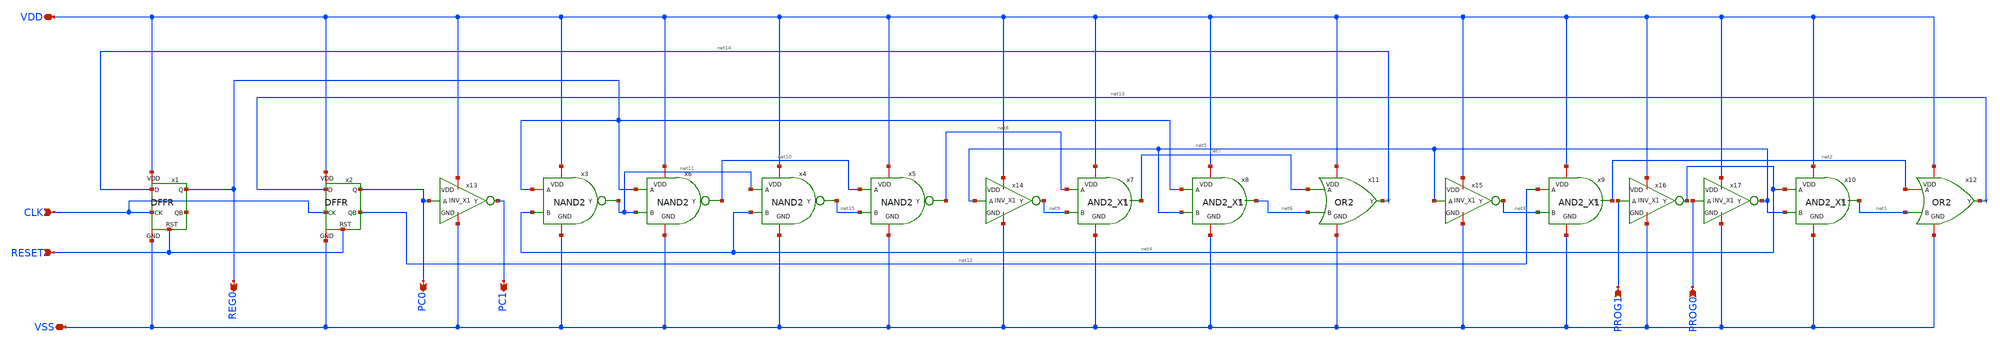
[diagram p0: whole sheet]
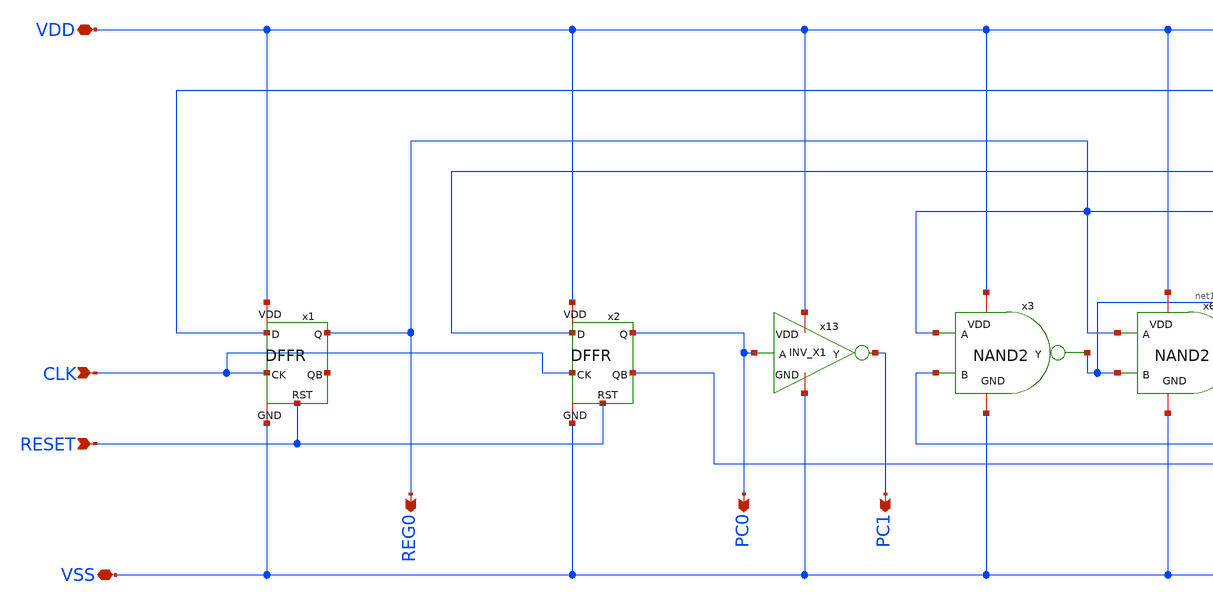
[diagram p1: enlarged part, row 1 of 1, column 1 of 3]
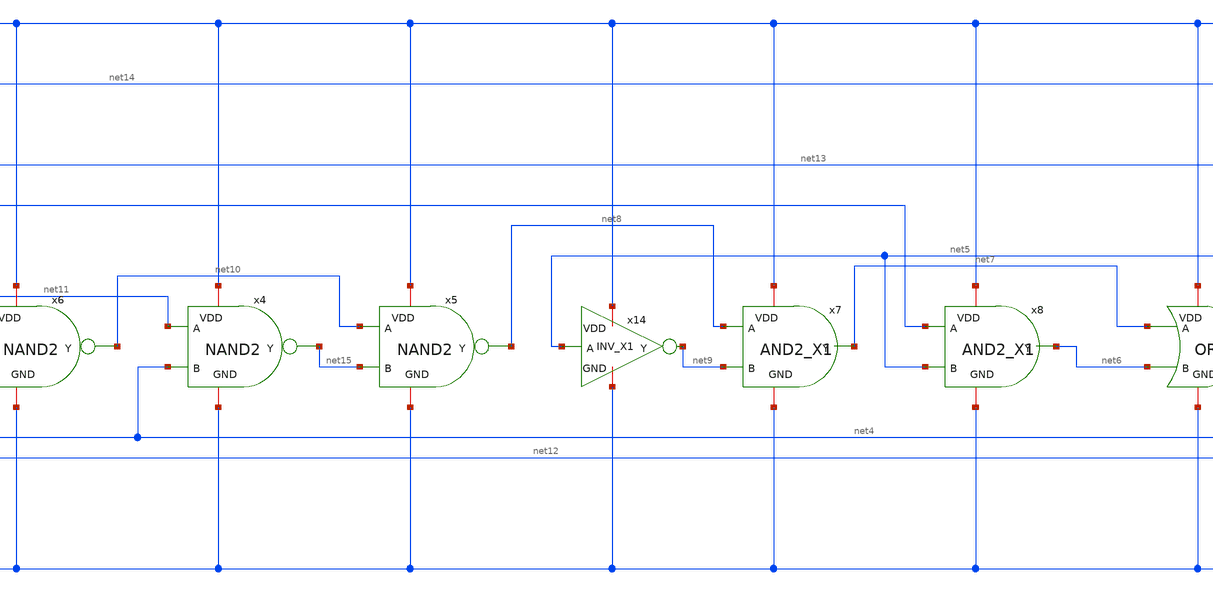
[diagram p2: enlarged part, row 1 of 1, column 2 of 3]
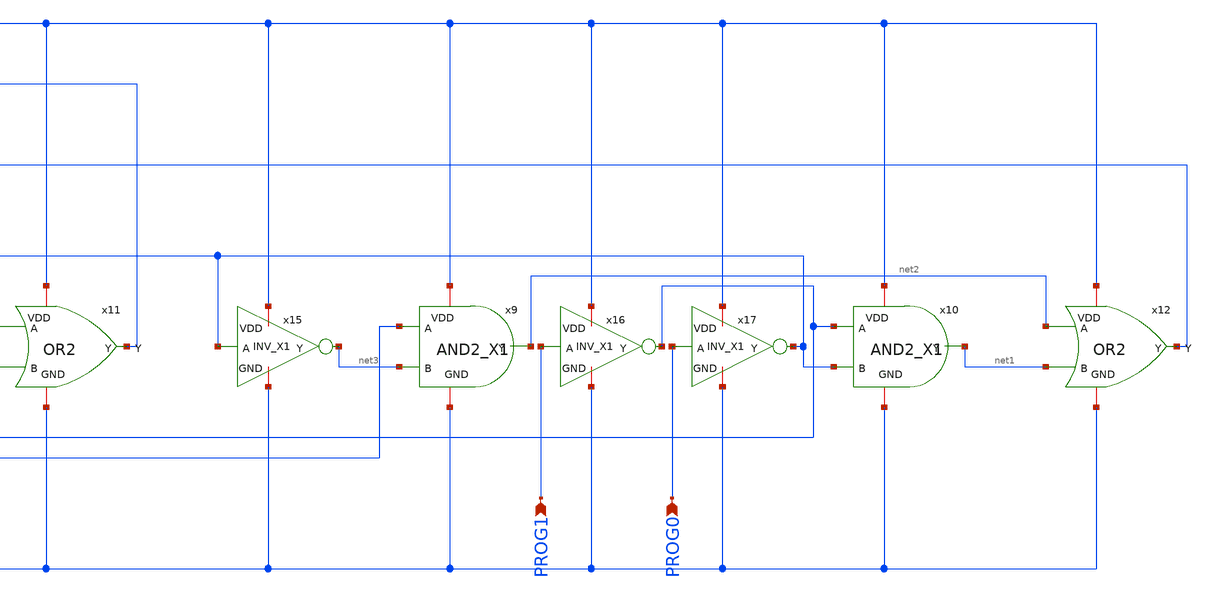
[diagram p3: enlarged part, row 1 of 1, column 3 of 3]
** sch_path: member_project/1bit-CPU/yamada3/1bit-CPU_1line_yamada3.sch
**.subckt 1bit-CPU_1line_yamada3 CLK RESET VDD VSS REG0 PC0 PC1 PROG1 PROG0
*.ipin CLK
*.ipin RESET
*.iopin VDD
*.iopin VSS
*.opin REG0
*.opin PC0
*.opin PC1
*.ipin PROG1
*.ipin PROG0
x1 VDD net16 net14 REG0 RESET VSS CLK DFFR
x2 VDD net12 net13 PC0 RESET VSS CLK DFFR
x13 VDD PC0 PC1 VSS INV_X1
x7 VDD net7 net8 net9 VSS AND2_X1
x8 VDD net6 REG0 net5 VSS AND2_X1
x9 VDD net2 net12 net3 VSS AND2_X1
x10 VDD net1 net4 net5 VSS AND2_X1
x11 VDD net14 net7 net6 VSS OR2
x12 VDD net13 net2 net1 VSS OR2
x14 VDD net5 net9 VSS INV_X1
x15 VDD net5 net3 VSS INV_X1
x16 VDD PROG1 net4 VSS INV_X1
x17 VDD PROG0 net5 VSS INV_X1
x3 VDD net11 REG0 net4 VSS NAND2
x4 VDD net15 net11 net4 VSS NAND2
x5 VDD net8 net10 net15 VSS NAND2
x6 VDD net10 REG0 net11 VSS NAND2
**.ends

* expanding   symbol:  IP62_5_stdcell/DFFR.sym # of pins=7
** sym_path: IP62_5_stdcell/DFFR.sym
** sch_path: IP62_5_stdcell/DFFR.sch
.subckt DFFR VDD QB D Q RST GND CK
*.iopin VDD
*.iopin GND
*.ipin CK
*.ipin D
*.opin Q
*.opin QB
*.ipin RST
XM2 net2 D VDD VDD PMOS w=10.2u l=1u as=0 ad=0 ps=0 pd=0 nrd=0 nrs=0 m=1
XM1 net3 CLK net2 VDD PMOS w=10.2u l=1u as=0 ad=0 ps=0 pd=0 nrd=0 nrs=0 m=1
XM11 net5 net8 VDD VDD PMOS w=10.2u l=1u as=0 ad=0 ps=0 pd=0 nrd=0 nrs=0 m=1
XM12 net3 CKB net5 VDD PMOS w=10.2u l=1u as=0 ad=0 ps=0 pd=0 nrd=0 nrs=0 m=1
XM15 net7 net3 VDD VDD PMOS w=10.2u l=1u as=0 ad=0 ps=0 pd=0 nrd=0 nrs=0 m=1
XM16 net8 RST net7 VDD PMOS w=10.2u l=1u as=0 ad=0 ps=0 pd=0 nrd=0 nrs=0 m=1
XM18 net9 net8 VDD VDD PMOS w=10.2u l=1u as=0 ad=0 ps=0 pd=0 nrd=0 nrs=0 m=1
XM19 net10 CKB net9 VDD PMOS w=10.2u l=1u as=0 ad=0 ps=0 pd=0 nrd=0 nrs=0 m=1
XM23 net12 net14 VDD VDD PMOS w=10.2u l=1u as=0 ad=0 ps=0 pd=0 nrd=0 nrs=0 m=1
XM24 net10 CLK net12 VDD PMOS w=10.2u l=1u as=0 ad=0 ps=0 pd=0 nrd=0 nrs=0 m=1
XM27 net15 net10 VDD VDD PMOS w=10.2u l=1u as=0 ad=0 ps=0 pd=0 nrd=0 nrs=0 m=1
XM28 net14 RST net15 VDD PMOS w=10.2u l=1u as=0 ad=0 ps=0 pd=0 nrd=0 nrs=0 m=1
XM31 QB net14 VDD VDD PMOS w=10.2u l=1u as=0 ad=0 ps=0 pd=0 nrd=0 nrs=0 m=1
XM33 Q QB VDD VDD PMOS w=10.2u l=1u as=0 ad=0 ps=0 pd=0 nrd=0 nrs=0 m=1
XM35 QB net14 GND GND NMOS w=3.4u l=1u as=0 ad=0 ps=0 pd=0 nrd=0 nrs=0 m=1
XM32 Q QB GND GND NMOS w=3.4u l=1u as=0 ad=0 ps=0 pd=0 nrd=0 nrs=0 m=1
XM29 net14 RST GND GND NMOS w=3.4u l=1u as=0 ad=0 ps=0 pd=0 nrd=0 nrs=0 m=1
XM30 net14 net10 GND GND NMOS w=3.4u l=1u as=0 ad=0 ps=0 pd=0 nrd=0 nrs=0 m=1
XM25 net10 CKB net13 GND NMOS w=3.4u l=1u as=0 ad=0 ps=0 pd=0 nrd=0 nrs=0 m=1
XM26 net13 net14 GND GND NMOS w=3.4u l=1u as=0 ad=0 ps=0 pd=0 nrd=0 nrs=0 m=1
XM20 net10 CLK net11 GND NMOS w=3.4u l=1u as=0 ad=0 ps=0 pd=0 nrd=0 nrs=0 m=1
XM21 net11 net8 GND GND NMOS w=3.4u l=1u as=0 ad=0 ps=0 pd=0 nrd=0 nrs=0 m=1
XM17 net8 net3 GND GND NMOS w=3.4u l=1u as=0 ad=0 ps=0 pd=0 nrd=0 nrs=0 m=1
XM22 net8 RST GND GND NMOS w=3.4u l=1u as=0 ad=0 ps=0 pd=0 nrd=0 nrs=0 m=1
XM13 net3 CLK net6 GND NMOS w=3.4u l=1u as=0 ad=0 ps=0 pd=0 nrd=0 nrs=0 m=1
XM14 net6 net8 GND GND NMOS w=3.4u l=1u as=0 ad=0 ps=0 pd=0 nrd=0 nrs=0 m=1
XM7 net3 CKB net4 GND NMOS w=3.4u l=1u as=0 ad=0 ps=0 pd=0 nrd=0 nrs=0 m=1
XM8 net4 D GND GND NMOS w=3.4u l=1u as=0 ad=0 ps=0 pd=0 nrd=0 nrs=0 m=1
XM3 net1 CK VDD VDD PMOS w=10.2u l=1u as=0 ad=0 ps=0 pd=0 nrd=0 nrs=0 m=1
XM4 CLK net1 VDD VDD PMOS w=10.2u l=1u as=0 ad=0 ps=0 pd=0 nrd=0 nrs=0 m=1
XM5 CKB CLK VDD VDD PMOS w=10.2u l=1u as=0 ad=0 ps=0 pd=0 nrd=0 nrs=0 m=1
XM34 net1 CK GND GND NMOS w=3.4u l=1u as=0 ad=0 ps=0 pd=0 nrd=0 nrs=0 m=1
XM6 CLK net1 GND GND NMOS w=3.4u l=1u as=0 ad=0 ps=0 pd=0 nrd=0 nrs=0 m=1
XM9 CKB CLK GND GND NMOS w=3.4u l=1u as=0 ad=0 ps=0 pd=0 nrd=0 nrs=0 m=1
.ends


* expanding   symbol:  IP62_5_stdcell/INV_X1.sym # of pins=4
** sym_path: IP62_5_stdcell/INV_X1.sym
** sch_path: IP62_5_stdcell/INV_X1.sch
.subckt INV_X1 VDD A Y GND
*.ipin A
*.opin Y
*.iopin GND
*.iopin VDD
XM7 Y A VDD VDD PMOS w=10.2u l=1u as=0 ad=0 ps=0 pd=0 nrd=0 nrs=0 m=1
XM2 Y A GND GND NMOS w=3.4u l=1u as=0 ad=0 ps=0 pd=0 nrd=0 nrs=0 m=1
.ends


* expanding   symbol:  IP62_5_stdcell/AND2_X1.sym # of pins=5
** sym_path: IP62_5_stdcell/AND2_X1.sym
** sch_path: IP62_5_stdcell/AND2_X1.sch
.subckt AND2_X1 VDD Y A B GND
*.opin Y
*.ipin A
*.ipin B
*.iopin VDD
*.iopin GND
XM7 net1 B VDD VDD PMOS w=10.2u l=1u as=0 ad=0 ps=0 pd=0 nrd=0 nrs=0 m=1
XM1 net1 A VDD VDD PMOS w=10.2u l=1u as=0 ad=0 ps=0 pd=0 nrd=0 nrs=0 m=1
XM2 Y net1 VDD VDD PMOS w=10.2u l=1u as=0 ad=0 ps=0 pd=0 nrd=0 nrs=0 m=1
XM3 Y net1 GND GND NMOS w=3.4u l=1u as=0 ad=0 ps=0 pd=0 nrd=0 nrs=0 m=1
XM4 net1 A net2 GND NMOS w=3.4u l=1u as=0 ad=0 ps=0 pd=0 nrd=0 nrs=0 m=1
XM5 net2 B GND GND NMOS w=3.4u l=1u as=0 ad=0 ps=0 pd=0 nrd=0 nrs=0 m=1
.ends


* expanding   symbol:  IP62_5_stdcell/OR2.sym # of pins=5
** sym_path: IP62_5_stdcell/OR2.sym
** sch_path: IP62_5_stdcell/OR2.sch
.subckt OR2 VDD Y A B GND
*.ipin A
*.ipin B
*.opin Y
*.iopin VDD
*.iopin GND
XM7 net2 B VDD VDD PMOS w=10.2u l=1u as=0 ad=0 ps=0 pd=0 nrd=0 nrs=0 m=1
XM2 net1 A net2 VDD PMOS w=10.2u l=1u as=0 ad=0 ps=0 pd=0 nrd=0 nrs=0 m=1
XM4 Y net1 VDD VDD PMOS w=10.2u l=1u as=0 ad=0 ps=0 pd=0 nrd=0 nrs=0 m=1
XM1 net1 B GND GND NMOS w=3.4u l=1u as=0 ad=0 ps=0 pd=0 nrd=0 nrs=0 m=1
XM3 net1 A GND GND NMOS w=3.4u l=1u as=0 ad=0 ps=0 pd=0 nrd=0 nrs=0 m=1
XM5 Y net1 GND GND NMOS w=3.4u l=1u as=0 ad=0 ps=0 pd=0 nrd=0 nrs=0 m=1
.ends


* expanding   symbol:  IP62_5_stdcell/NAND2.sym # of pins=5
** sym_path: IP62_5_stdcell/NAND2.sym
** sch_path: IP62_5_stdcell/NAND2.sch
.subckt NAND2 VDD Y A B GND
*.ipin B
*.ipin A
*.opin Y
*.iopin GND
*.iopin VDD
XM7 Y A VDD VDD PMOS w=10.2u l=1u as=0 ad=0 ps=0 pd=0 nrd=0 nrs=0 m=1
XM1 Y B VDD VDD PMOS w=10.2u l=1u as=0 ad=0 ps=0 pd=0 nrd=0 nrs=0 m=1
XM2 Y B net1 GND NMOS w=3.4u l=1u as=0 ad=0 ps=0 pd=0 nrd=0 nrs=0 m=1
XM3 net1 A GND GND NMOS w=3.4u l=1u as=0 ad=0 ps=0 pd=0 nrd=0 nrs=0 m=1
.ends

.end
